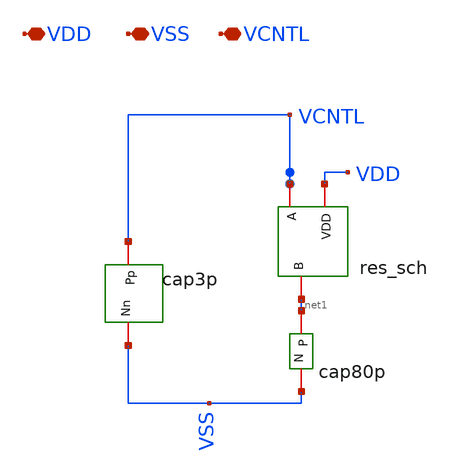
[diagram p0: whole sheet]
** sch_path: Clock_Generator_PAKISTAN_02/Schematics/LF.sch
**.subckt LF VSS VCNTL VDD
*.iopin VSS
*.iopin VCNTL
*.iopin VDD
x1 VCNTL net1 VDD res_sch
x2 VSS net1 cap80p
x3 VSS VCNTL cap3p
**.ends

* expanding   symbol:  res_sch.sym # of pins=3
** sym_path: Clock_Generator_PAKISTAN_02/Schematics/res_sch.sym
** sch_path: Clock_Generator_PAKISTAN_02/Schematics/res_sch.sch
.subckt res_sch A B VDD
*.iopin VDD
*.iopin A
*.iopin B
XR1 B A VDD ppolyf_u r_width=0.8e-6 r_length=100e-6 m=1
.ends


* expanding   symbol:  cap80p.sym # of pins=2
** sym_path: Clock_Generator_PAKISTAN_02/xschem/cap80p.sym
** sch_path: Clock_Generator_PAKISTAN_02/xschem/cap80p.sch
.subckt cap80p N P
*.iopin P
*.iopin N
XC1 P N cap_mim_2f0_m4m5_noshield c_width=25e-6 c_length=25e-6 m=64
.ends


* expanding   symbol:  cap3p.sym # of pins=2
** sym_path: Clock_Generator_PAKISTAN_02/Schematics/cap3p.sym
** sch_path: Clock_Generator_PAKISTAN_02/Schematics/cap3p.sch
.subckt cap3p Nn Pp
*.iopin Pp
*.iopin Nn
XC1 Pp Nn cap_mim_2f0_m4m5_noshield c_width=42.5e-6 c_length=42.5e-6 m=1
.ends

.end
